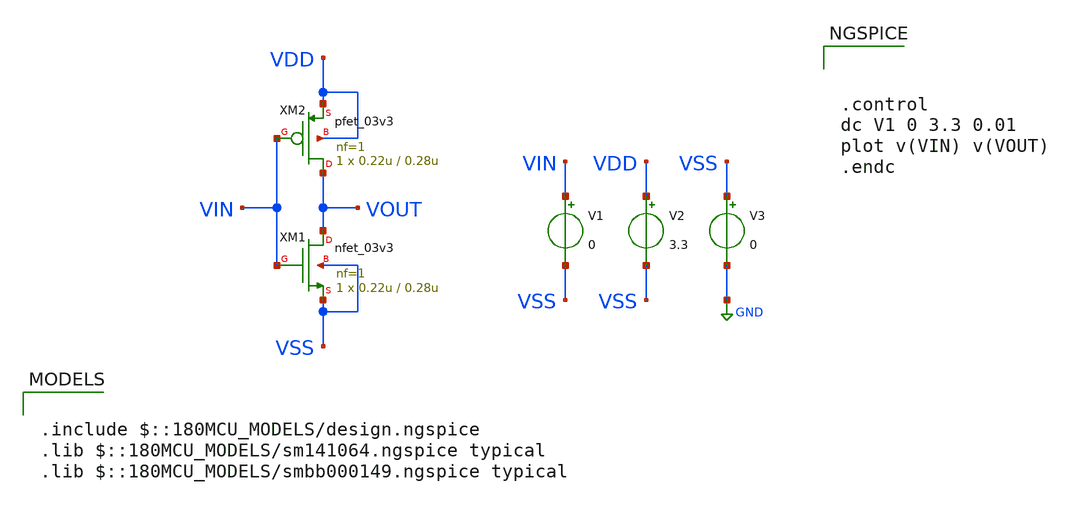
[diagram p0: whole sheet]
** sch_path: week01_mosfet_cmos/tugas2_cmos_inverter/cmos-inverter.sch
**.subckt cmos-inverter
V1 VIN VSS 0
V2 VDD VSS 3.3
V3 VSS GND 0
XM1 VOUT VIN VSS VSS nfet_03v3 L=0.28u W=0.22u nf=1 ad='int((nf+1)/2) * W/nf * 0.18u' as='int((nf+2)/2) * W/nf * 0.18u'
+ pd='2*int((nf+1)/2) * (W/nf + 0.18u)' ps='2*int((nf+2)/2) * (W/nf + 0.18u)' nrd='0.18u / W' nrs='0.18u / W'
+ sa=0 sb=0 sd=0 m=1
XM2 VOUT VIN VDD VDD pfet_03v3 L=0.28u W=0.22u nf=1 ad='int((nf+1)/2) * W/nf * 0.18u' as='int((nf+2)/2) * W/nf * 0.18u'
+ pd='2*int((nf+1)/2) * (W/nf + 0.18u)' ps='2*int((nf+2)/2) * (W/nf + 0.18u)' nrd='0.18u / W' nrs='0.18u / W'
+ sa=0 sb=0 sd=0 m=1
**** begin user architecture code



.control
dc V1 0 3.3 0.01
plot v(VIN) v(VOUT)
.endc



.include $::180MCU_MODELS/design.ngspice
.lib $::180MCU_MODELS/sm141064.ngspice typical
.lib $::180MCU_MODELS/smbb000149.ngspice typical

**** end user architecture code
**.ends
.GLOBAL GND
.end
